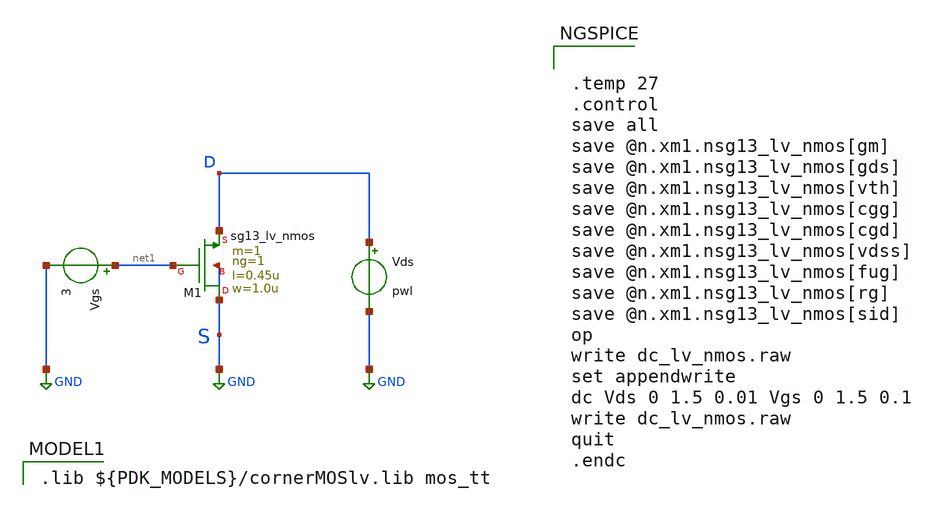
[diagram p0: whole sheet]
** sch_path: Single_MOS_sims/LV_NMOS_TB.sch
**.subckt LV_NMOS_TB
XM1 GND net1 D GND sg13_lv_nmos w=1.0u l=0.45u ng=1 m=1 mm_ok=1
Vgs net1 GND 3
Vds D GND pwl
**** begin user architecture code
 .lib cornerMOSlv.lib mos_tt

 .lib ${PDK_MODELS}/cornerMOSlv.lib mos_tt



.temp 27
.control
save all
save @n.xm1.nsg13_lv_nmos[gm]
save @n.xm1.nsg13_lv_nmos[gds]
save @n.xm1.nsg13_lv_nmos[vth]
save @n.xm1.nsg13_lv_nmos[cgg]
save @n.xm1.nsg13_lv_nmos[cgd]
save @n.xm1.nsg13_lv_nmos[vdss]
save @n.xm1.nsg13_lv_nmos[fug]
save @n.xm1.nsg13_lv_nmos[rg]
save @n.xm1.nsg13_lv_nmos[sid]
op
write dc_lv_nmos.raw
set appendwrite
dc Vds 0 1.5 0.01 Vgs 0 1.5 0.1
write dc_lv_nmos.raw
quit
.endc


**** end user architecture code
**.ends
.GLOBAL GND
.end
